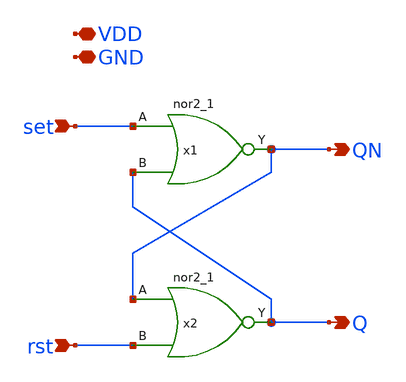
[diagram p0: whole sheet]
** sch_path: design/xschem/srlatch.sch
**.subckt srlatch set rst Q QN VDD GND
*.ipin set
*.ipin rst
*.opin Q
*.opin QN
*.iopin VDD
*.iopin GND
x1 set Q GND GND VDD VDD QN sky130_fd_sc_hd__nor2_1
x2 QN rst GND GND VDD VDD Q sky130_fd_sc_hd__nor2_1
**.ends
.end
